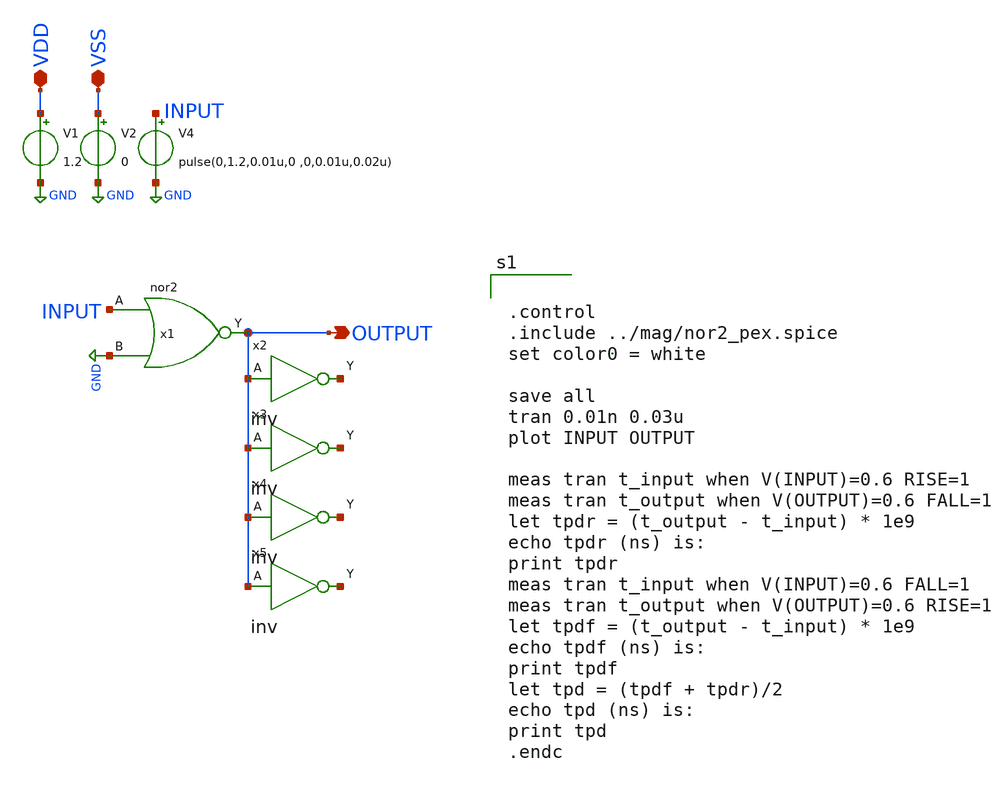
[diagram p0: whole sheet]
** sch_path: design/xschem/NOR/nor2_TB.sch
**.subckt nor2_TB OUTPUT VDD VSS
*.opin OUTPUT
*.iopin VDD
*.iopin VSS
V1 VDD GND 1.2
V2 VSS GND 0
V4 INPUT GND pulse(0,1.2,0.01u,0 ,0,0.01u,0.02u)
x2 OUTPUT VSS VDD net1 inv
x3 OUTPUT VSS VDD net2 inv
x4 OUTPUT VSS VDD net3 inv
x5 OUTPUT VSS VDD net4 inv
x1 INPUT GND VSS VDD OUTPUT nor2
**** begin user architecture code

** opencircuitdesign pdks install
.lib $::SKYWATER_MODELS/sky130.lib.spice tt_mm




.control
.include ../mag/nor2_pex.spice
set color0 = white

save all
tran 0.01n 0.03u
plot INPUT OUTPUT

meas tran t_input when V(INPUT)=0.6 RISE=1
meas tran t_output when V(OUTPUT)=0.6 FALL=1
let tpdr = (t_output - t_input) * 1e9
echo tpdr (ns) is:
print tpdr
meas tran t_input when V(INPUT)=0.6 FALL=1
meas tran t_output when V(OUTPUT)=0.6 RISE=1
let tpdf = (t_output - t_input) * 1e9
echo tpdf (ns) is:
print tpdf
let tpd = (tpdf + tpdr)/2
echo tpd (ns) is:
print tpd
.endc


**** end user architecture code
**.ends
.GLOBAL GND
.end
